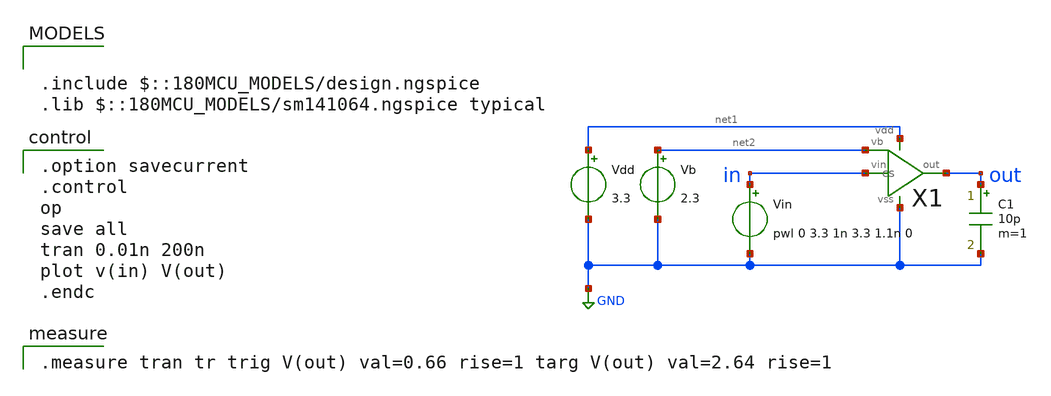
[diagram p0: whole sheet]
** sch_path: opamp/cs_tran.sch
**.subckt cs_tran
Vdd net1 GND 3.3
Vb net2 GND 2.3
X1 in net2 out net1 GND cs
C1 out GND 10p m=1
Vin in GND pwl 0 3.3 1n 3.3 1.1n 0
**** begin user architecture code

.include $::180MCU_MODELS/design.ngspice
.lib $::180MCU_MODELS/sm141064.ngspice typical


.option savecurrent
.control
op
save all
tran 0.01n 200n
plot v(in) V(out)
.endc


.measure tran tr trig V(out) val=0.66 rise=1 targ V(out) val=2.64 rise=1

**** end user architecture code
**.ends

* expanding   symbol:  cs.sym # of pins=5
** sym_path: cs.sym
** sch_path: cs.sch
.subckt cs vin vb out vdd vss
*.ipin vb
*.ipin vin
*.opin out
*.iopin vss
*.iopin vdd
XM6 out vb vdd vdd pfet_03v3 L=0.28u W=56u nf=1 ad='int((nf+1)/2) * W/nf * 0.18u' as='int((nf+2)/2) * W/nf * 0.18u'
+ pd='2*int((nf+1)/2) * (W/nf + 0.18u)' ps='2*int((nf+2)/2) * (W/nf + 0.18u)' nrd='0.18u / W' nrs='0.18u / W'
+ sa=0 sb=0 sd=0 m=1
XM7 out vin vss vss nfet_03v3 L=0.28u W=28u nf=1 ad='int((nf+1)/2) * W/nf * 0.18u' as='int((nf+2)/2) * W/nf * 0.18u'
+ pd='2*int((nf+1)/2) * (W/nf + 0.18u)' ps='2*int((nf+2)/2) * (W/nf + 0.18u)' nrd='0.18u / W' nrs='0.18u / W'
+ sa=0 sb=0 sd=0 m=1
.ends

.GLOBAL GND
.end
